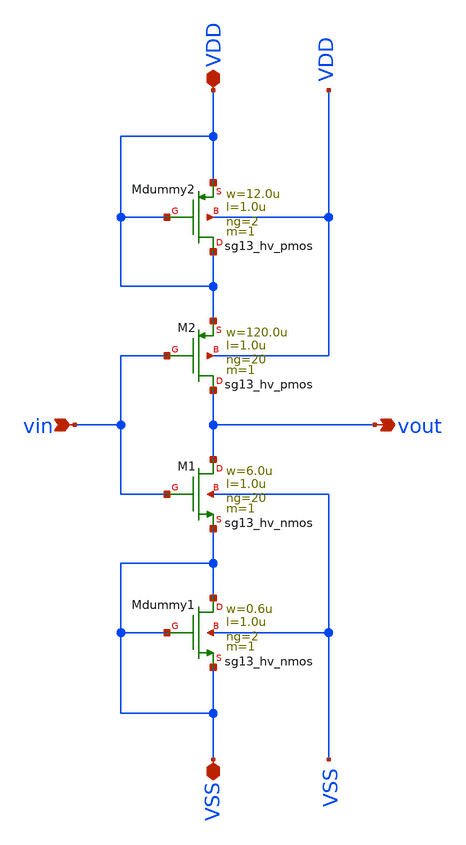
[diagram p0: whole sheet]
** sch_path: macros/heichips26_vcr/macros/switched_capacitor/schematic/xschem/high_th_inverter.sch
**.subckt high_th_inverter vin VDD VSS vout
*.ipin vin
*.iopin VDD
*.iopin VSS
*.opin vout
XMdummy1 VSS VSS VSS VSS sg13_hv_nmos w=0.6u l=1.0u ng=2 m=1 mm_ok=1
XMdummy2 VDD VDD VDD VDD sg13_hv_pmos w=12.0u l=1.0u ng=2 m=1 mm_ok=1
XM1 vout vin VSS VSS sg13_hv_nmos w=6.0u l=1.0u ng=20 m=1 mm_ok=1
XM2 vout vin VDD VDD sg13_hv_pmos w=120.0u l=1.0u ng=20 m=1 mm_ok=1
**.ends
.end
